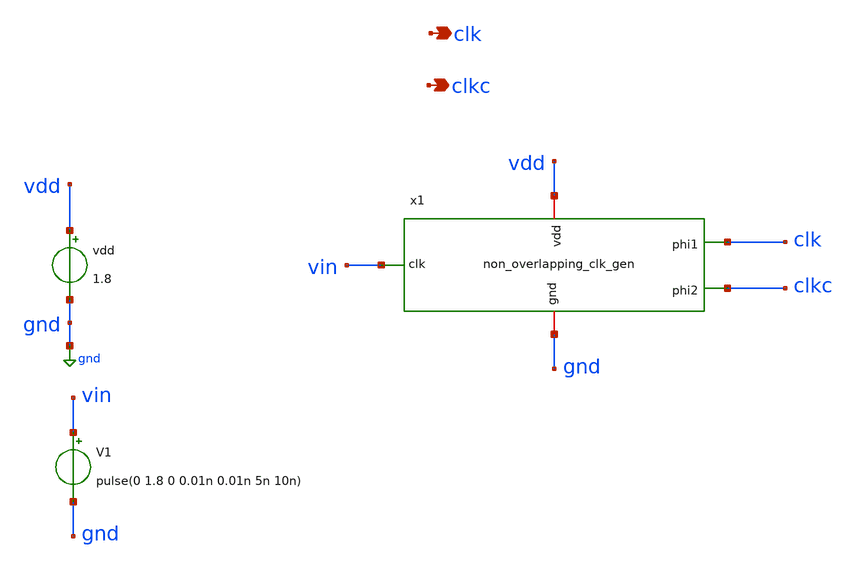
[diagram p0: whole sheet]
** sch_path: SequentialCircuits/Non Overlapping Clock Generator/non_overlapping_clk_gen_tb.sch
**.subckt non_overlapping_clk_gen_tb clk clkc
*.opin clk
*.opin clkc
x1 vdd clk vin clkc gnd non_overlapping_clk_gen
V1 vin gnd pulse(0 1.8 0 0.01n 0.01n 5n 10n)
vdd vdd gnd 1.8
**** begin user architecture code


.lib /usr/local/share/pdk/sky130A/libs.tech/ngspice/sky130.lib.spice tt
.control
    tran 0.01n 100n
    plot clk clkc
.endc

.save all

**** end user architecture code
**.ends

* expanding   symbol:  SequentialCircuits/D_ff/Non Overlapping Clock
*+ Generator/non_overlapping_clk_gen.sym # of pins=5
** sym_path: SequentialCircuits/Non Overlapping Clock Generator/non_overlapping_clk_gen.sym
** sch_path: SequentialCircuits/Non Overlapping Clock Generator/non_overlapping_clk_gen.sch
.subckt non_overlapping_clk_gen vdd phi1 clk phi2 gnd
*.ipin clk
*.iopin vdd
*.iopin gnd
*.opin phi1
*.opin phi2
x1 vdd gnd clk net1 not
x2 vdd gnd net1 phi2 phi1 nor
x3 vdd gnd phi1 clk phi2 nor
.ends


* expanding   symbol:  LogicGates/not.sym # of pins=4
** sym_path: LogicGates/not.sym
** sch_path: LogicGates/not.sch
.subckt not vdd gnd vin vout
*.ipin vin
*.iopin vdd
*.iopin gnd
*.opin vout
XM2 vout vin vdd vdd sky130_fd_pr__pfet_01v8 L=0.15 W=2 nf=1 ad='int((nf+1)/2) * W/nf * 0.29' as='int((nf+2)/2) * W/nf * 0.29'
+ pd='2*int((nf+1)/2) * (W/nf + 0.29)' ps='2*int((nf+2)/2) * (W/nf + 0.29)' nrd='0.29 / W' nrs='0.29 / W'
+ sa=0 sb=0 sd=0 mult=1 m=1
XM1 vout vin gnd gnd sky130_fd_pr__nfet_01v8 L=0.15 W=1 nf=1 ad='int((nf+1)/2) * W/nf * 0.29' as='int((nf+2)/2) * W/nf * 0.29'
+ pd='2*int((nf+1)/2) * (W/nf + 0.29)' ps='2*int((nf+2)/2) * (W/nf + 0.29)' nrd='0.29 / W' nrs='0.29 / W'
+ sa=0 sb=0 sd=0 mult=1 m=1
.ends


* expanding   symbol:  LogicGates/nor.sym # of pins=5
** sym_path: LogicGates/nor.sym
** sch_path: LogicGates/nor.sch
.subckt nor vdd gnd A B Y
*.ipin A
*.ipin B
*.iopin vdd
*.iopin gnd
*.opin Y
XM1 Y A gnd gnd sky130_fd_pr__nfet_01v8 L=0.15 W=1 nf=1 ad='int((nf+1)/2) * W/nf * 0.29' as='int((nf+2)/2) * W/nf * 0.29'
+ pd='2*int((nf+1)/2) * (W/nf + 0.29)' ps='2*int((nf+2)/2) * (W/nf + 0.29)' nrd='0.29 / W' nrs='0.29 / W'
+ sa=0 sb=0 sd=0 mult=1 m=1
XM2 Y B gnd gnd sky130_fd_pr__nfet_01v8 L=0.15 W=1 nf=1 ad='int((nf+1)/2) * W/nf * 0.29' as='int((nf+2)/2) * W/nf * 0.29'
+ pd='2*int((nf+1)/2) * (W/nf + 0.29)' ps='2*int((nf+2)/2) * (W/nf + 0.29)' nrd='0.29 / W' nrs='0.29 / W'
+ sa=0 sb=0 sd=0 mult=1 m=1
XM3 net1 A vdd vdd sky130_fd_pr__pfet_01v8 L=0.15 W=2 nf=1 ad='int((nf+1)/2) * W/nf * 0.29' as='int((nf+2)/2) * W/nf * 0.29'
+ pd='2*int((nf+1)/2) * (W/nf + 0.29)' ps='2*int((nf+2)/2) * (W/nf + 0.29)' nrd='0.29 / W' nrs='0.29 / W'
+ sa=0 sb=0 sd=0 mult=1 m=1
XM4 Y B net1 vdd sky130_fd_pr__pfet_01v8 L=0.15 W=2 nf=1 ad='int((nf+1)/2) * W/nf * 0.29' as='int((nf+2)/2) * W/nf * 0.29'
+ pd='2*int((nf+1)/2) * (W/nf + 0.29)' ps='2*int((nf+2)/2) * (W/nf + 0.29)' nrd='0.29 / W' nrs='0.29 / W'
+ sa=0 sb=0 sd=0 mult=1 m=1
.ends

.GLOBAL gnd
.end
